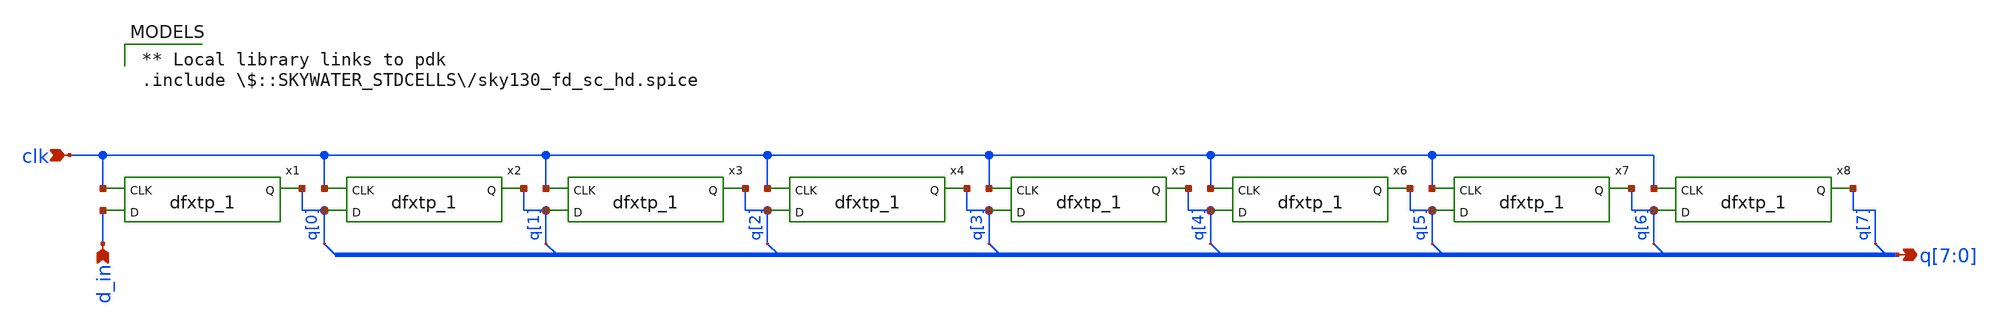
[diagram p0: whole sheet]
** sch_path: xschem/cfg_shift_register.sch
 ** Local library links to pdk
.include $::SKYWATER_STDCELLS/sky130_fd_sc_hd.spice

**.subckt cfg_shift_register clk d_in q[7],q[6],q[5],q[4],q[3],q[2],q[1],q[0]
*.ipin clk
*.ipin d_in
*.opin q[7],q[6],q[5],q[4],q[3],q[2],q[1],q[0]
x1 clk d_in GND GND VDD VDD q[0] sky130_fd_sc_hd__dfxtp_1
x2 clk q[0] GND GND VDD VDD q[1] sky130_fd_sc_hd__dfxtp_1
x3 clk q[1] GND GND VDD VDD q[2] sky130_fd_sc_hd__dfxtp_1
x4 clk q[2] GND GND VDD VDD q[3] sky130_fd_sc_hd__dfxtp_1
x5 clk q[3] GND GND VDD VDD q[4] sky130_fd_sc_hd__dfxtp_1
x6 clk q[4] GND GND VDD VDD q[5] sky130_fd_sc_hd__dfxtp_1
x7 clk q[5] GND GND VDD VDD q[6] sky130_fd_sc_hd__dfxtp_1
x8 clk q[6] GND GND VDD VDD q[7] sky130_fd_sc_hd__dfxtp_1
**.ends
.end
